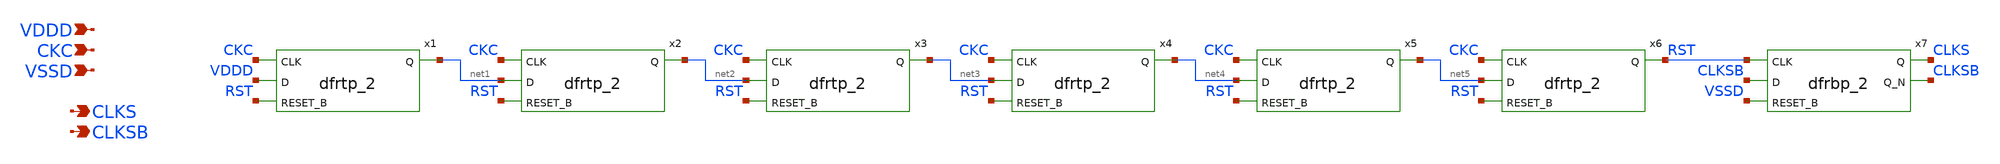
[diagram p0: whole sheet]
** sch_path: xschem/auto_sampling.sch
**.subckt auto_sampling CKC VDDD VSSD CLKS CLKSB
*.ipin CKC
*.ipin VDDD
*.ipin VSSD
*.opin CLKS
*.opin CLKSB
x1 CKC VDDD RST VSSD VSSD VDDD VDDD net1 sky130_fd_sc_hd__dfrtp_2
x2 CKC net1 RST VSSD VSSD VDDD VDDD net2 sky130_fd_sc_hd__dfrtp_2
x3 CKC net2 RST VSSD VSSD VDDD VDDD net3 sky130_fd_sc_hd__dfrtp_2
x4 CKC net3 RST VSSD VSSD VDDD VDDD net4 sky130_fd_sc_hd__dfrtp_2
x5 CKC net4 RST VSSD VSSD VDDD VDDD net5 sky130_fd_sc_hd__dfrtp_2
x6 CKC net5 RST VSSD VSSD VDDD VDDD RST sky130_fd_sc_hd__dfrtp_2
x7 RST CLKSB VSSD VSSD VSSD VDDD VDDD CLKS CLKSB sky130_fd_sc_hd__dfrbp_2
**.ends
.end
